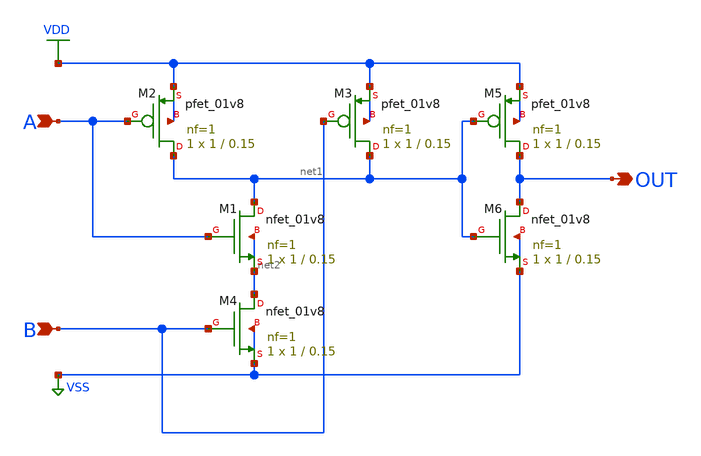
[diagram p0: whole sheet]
** sch_path: APIC-3/schematic/and_gate.sch
**.subckt and_gate A B OUT
*.ipin A
*.ipin B
*.opin OUT
XM1 net1 A net2 net2 sky130_fd_pr__nfet_01v8 L=0.15 W=1 nf=1 ad='int((nf+1)/2) * W/nf * 0.29' as='int((nf+2)/2) * W/nf * 0.29'
+ pd='2*int((nf+1)/2) * (W/nf + 0.29)' ps='2*int((nf+2)/2) * (W/nf + 0.29)' nrd='0.29 / W' nrs='0.29 / W'
+ sa=0 sb=0 sd=0 mult=1 m=1
XM4 net2 B VSS VSS sky130_fd_pr__nfet_01v8 L=0.15 W=1 nf=1 ad='int((nf+1)/2) * W/nf * 0.29' as='int((nf+2)/2) * W/nf * 0.29'
+ pd='2*int((nf+1)/2) * (W/nf + 0.29)' ps='2*int((nf+2)/2) * (W/nf + 0.29)' nrd='0.29 / W' nrs='0.29 / W'
+ sa=0 sb=0 sd=0 mult=1 m=1
XM6 OUT net1 VSS VSS sky130_fd_pr__nfet_01v8 L=0.15 W=1 nf=1 ad='int((nf+1)/2) * W/nf * 0.29' as='int((nf+2)/2) * W/nf * 0.29'
+ pd='2*int((nf+1)/2) * (W/nf + 0.29)' ps='2*int((nf+2)/2) * (W/nf + 0.29)' nrd='0.29 / W' nrs='0.29 / W'
+ sa=0 sb=0 sd=0 mult=1 m=1
XM2 net1 A VDD VDD sky130_fd_pr__pfet_01v8 L=0.15 W=1 nf=1 ad='int((nf+1)/2) * W/nf * 0.29' as='int((nf+2)/2) * W/nf * 0.29'
+ pd='2*int((nf+1)/2) * (W/nf + 0.29)' ps='2*int((nf+2)/2) * (W/nf + 0.29)' nrd='0.29 / W' nrs='0.29 / W'
+ sa=0 sb=0 sd=0 mult=1 m=1
XM3 net1 B VDD VDD sky130_fd_pr__pfet_01v8 L=0.15 W=1 nf=1 ad='int((nf+1)/2) * W/nf * 0.29' as='int((nf+2)/2) * W/nf * 0.29'
+ pd='2*int((nf+1)/2) * (W/nf + 0.29)' ps='2*int((nf+2)/2) * (W/nf + 0.29)' nrd='0.29 / W' nrs='0.29 / W'
+ sa=0 sb=0 sd=0 mult=1 m=1
XM5 OUT net1 VDD VDD sky130_fd_pr__pfet_01v8 L=0.15 W=1 nf=1 ad='int((nf+1)/2) * W/nf * 0.29' as='int((nf+2)/2) * W/nf * 0.29'
+ pd='2*int((nf+1)/2) * (W/nf + 0.29)' ps='2*int((nf+2)/2) * (W/nf + 0.29)' nrd='0.29 / W' nrs='0.29 / W'
+ sa=0 sb=0 sd=0 mult=1 m=1
**.ends
.GLOBAL VDD
.GLOBAL VSS
.end
